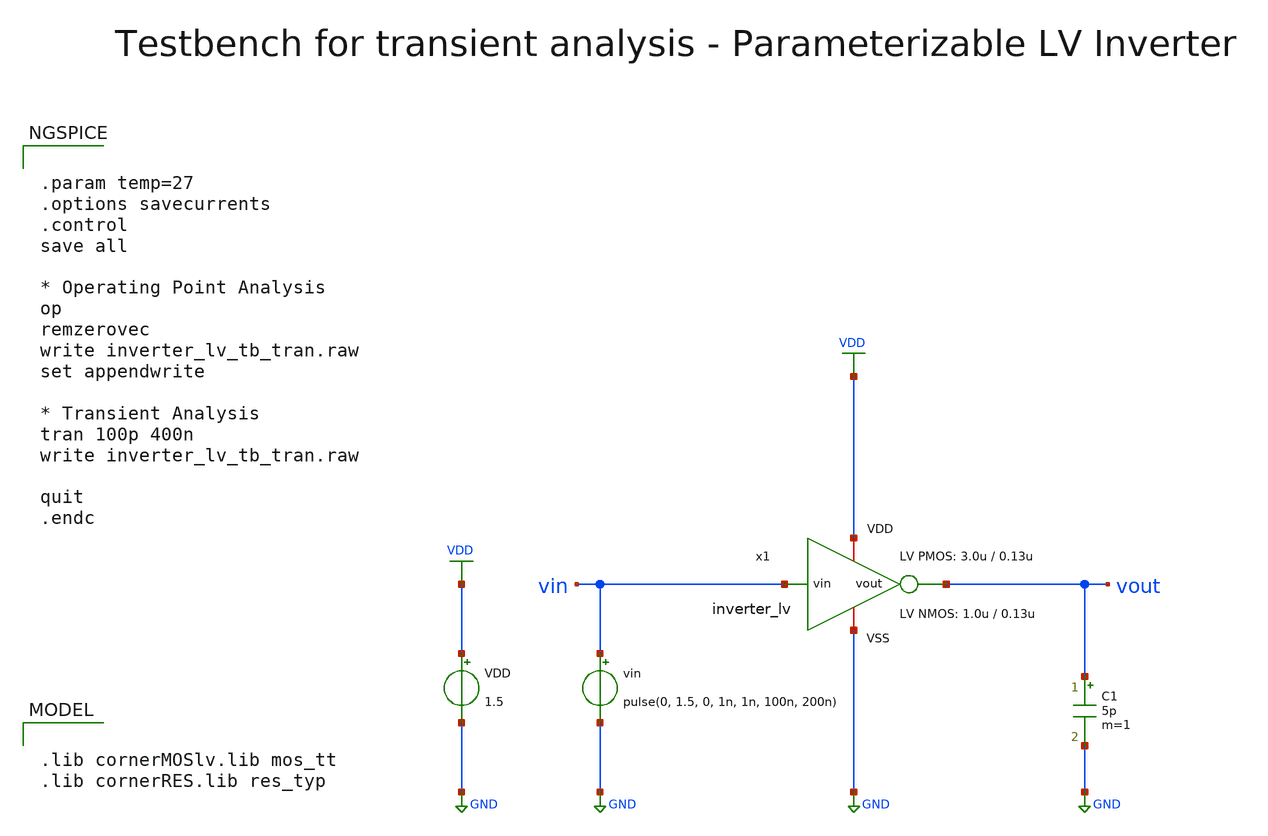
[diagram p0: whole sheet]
** sch_path: SG13G2_ATBS-ADC-main/xschem/inverter/testbenches/inverter_lv_tb_tran.sch
**.subckt inverter_lv_tb_tran
VDD VDD GND 1.5
vin vin GND pulse(0, 1.5, 0, 1n, 1n, 100n, 200n)
C1 vout GND 5p m=1
x1 VDD vin vout GND inverter_lv W_P=3.0u L_P=0.13u W_N=1.0u L_N=0.13u
**** begin user architecture code

.lib cornerMOSlv.lib mos_tt
.lib cornerRES.lib res_typ



.param temp=27
.options savecurrents
.control
save all

* Operating Point Analysis
op
remzerovec
write inverter_lv_tb_tran.raw
set appendwrite

* Transient Analysis
tran 100p 400n
write inverter_lv_tb_tran.raw

quit
.endc


**** end user architecture code
**.ends

* expanding   symbol:  inverter/inverter_lv.sym # of pins=4
** sym_path: SG13G2_ATBS-ADC-main/xschem/inverter/inverter_lv.sym
** sch_path: SG13G2_ATBS-ADC-main/xschem/inverter/inverter_lv.sch
.subckt inverter_lv VDD vin vout VSS  W_P=3.0u L_P=0.13u W_N=1.0u L_N=0.13u
*.ipin vin
*.iopin VDD
*.iopin VSS
*.opin vout
XM1 vout vin VDD VDD sg13_lv_pmos w=W_P l=L_P ng=1 m=1 mm_ok=1
XM2 vout vin VSS VSS sg13_lv_nmos w=W_N l=L_N ng=1 m=1 mm_ok=1
.ends

.GLOBAL GND
.GLOBAL VDD
.end
